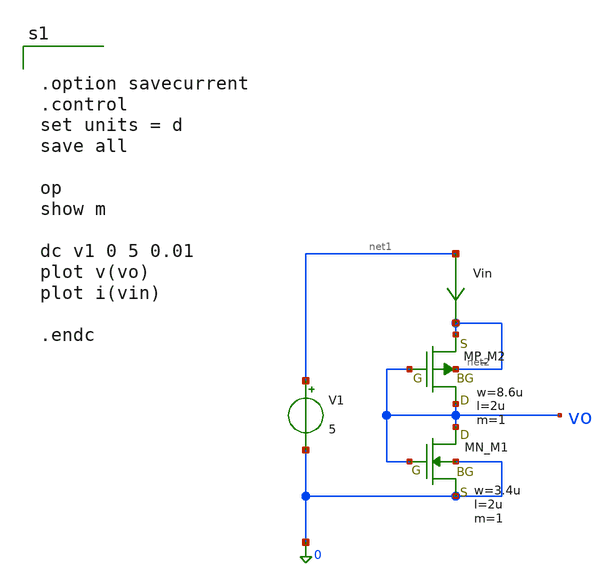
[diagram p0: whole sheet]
** sch_path: member_project/JJY_Receiver/Masahiro/jjy_recv/diff_amp/check_bias.sch
**.subckt check_bias
XM1 vo vo 0 0 NMOS w=3.4u l=2u as=0 ad=0 ps=0 pd=0 nrd=0 nrs=0 m=1
XM2 vo vo net2 net2 PMOS w=8.6u l=2u as=0 ad=0 ps=0 pd=0 nrd=0 nrs=0 m=1
V1 net1 0 5
Vin net1 net2 0
.save i(vin)
**** begin user architecture code
 .include $::LIB/ip62_models


.option savecurrent
.control
set units = d
save all

op
show m

dc v1 0 5 0.01
plot v(vo)
plot i(vin)

.endc


**** end user architecture code
**.ends
.end
